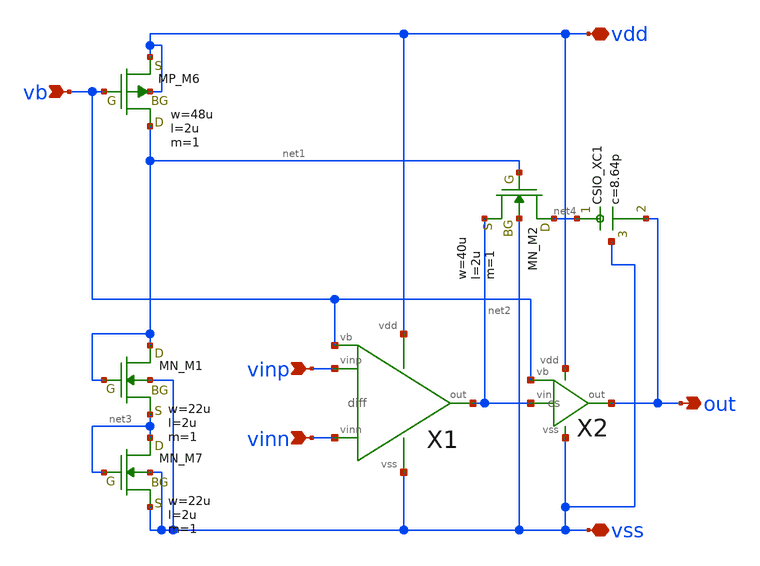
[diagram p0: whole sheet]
** sch_path: member_project/opamp/makoto645/testbench/2stage_pc.sch
**.subckt 2stage_pc vinp vinn vb out vdd vss
*.ipin vinp
*.ipin vinn
*.ipin vb
*.opin out
*.iopin vdd
*.iopin vss
X1 vinp vinn net2 vdd vss vb diff
X2 net2 vb out vdd vss cs
XM6 net1 vb vdd vdd PMOS w=48u l=2u as=0 ad=0 ps=0 pd=0 nrd=0 nrs=0 m=1
XM1 net1 net1 net3 vss NMOS w=22u l=2u as=0 ad=0 ps=0 pd=0 nrd=0 nrs=0 m=1
XM7 net3 net3 vss vss NMOS w=22u l=2u as=0 ad=0 ps=0 pd=0 nrd=0 nrs=0 m=1
XM2 net4 net1 net2 vss NMOS w=40u l=2u as=0 ad=0 ps=0 pd=0 nrd=0 nrs=0 m=1
XXC1 net4 out vss F_CSIO c=8.64p x=120u y=120u m=1
**.ends

* expanding   symbol:  diff.sym # of pins=6
** sym_path: diff.sym
** sch_path: diff.sch
.subckt diff vinp vinn out vdd vss vb
*.ipin vinn
*.ipin vinp
*.ipin vb
*.opin out
*.iopin vdd
*.iopin vss
XM5 net2 vb vdd vdd PMOS w=200u l=2u as=0 ad=0 ps=0 pd=0 nrd=0 nrs=0 m=1
XM1 net1 vinn net2 net2 PMOS w=100u l=2u as=0 ad=0 ps=0 pd=0 nrd=0 nrs=0 m=1
XM2 out vinp net2 net2 PMOS w=100u l=2u as=0 ad=0 ps=0 pd=0 nrd=0 nrs=0 m=1
XM3 net1 net1 vss vss NMOS w=50u l=2u as=0 ad=0 ps=0 pd=0 nrd=0 nrs=0 m=1
XM4 out net1 vss vss NMOS w=50u l=2u as=0 ad=0 ps=0 pd=0 nrd=0 nrs=0 m=1
.ends


* expanding   symbol:  cs.sym # of pins=5
** sym_path: cs.sym
** sch_path: cs.sch
.subckt cs vin vb out vdd vss
*.ipin vb
*.ipin vin
*.opin out
*.iopin vss
*.iopin vdd
XM6 out vb vdd vdd PMOS w=480u l=2u as=0 ad=0 ps=0 pd=0 nrd=0 nrs=0 m=1
XM7 out vin vss vss NMOS w=220u l=2u as=0 ad=0 ps=0 pd=0 nrd=0 nrs=0 m=1
.ends

.end
